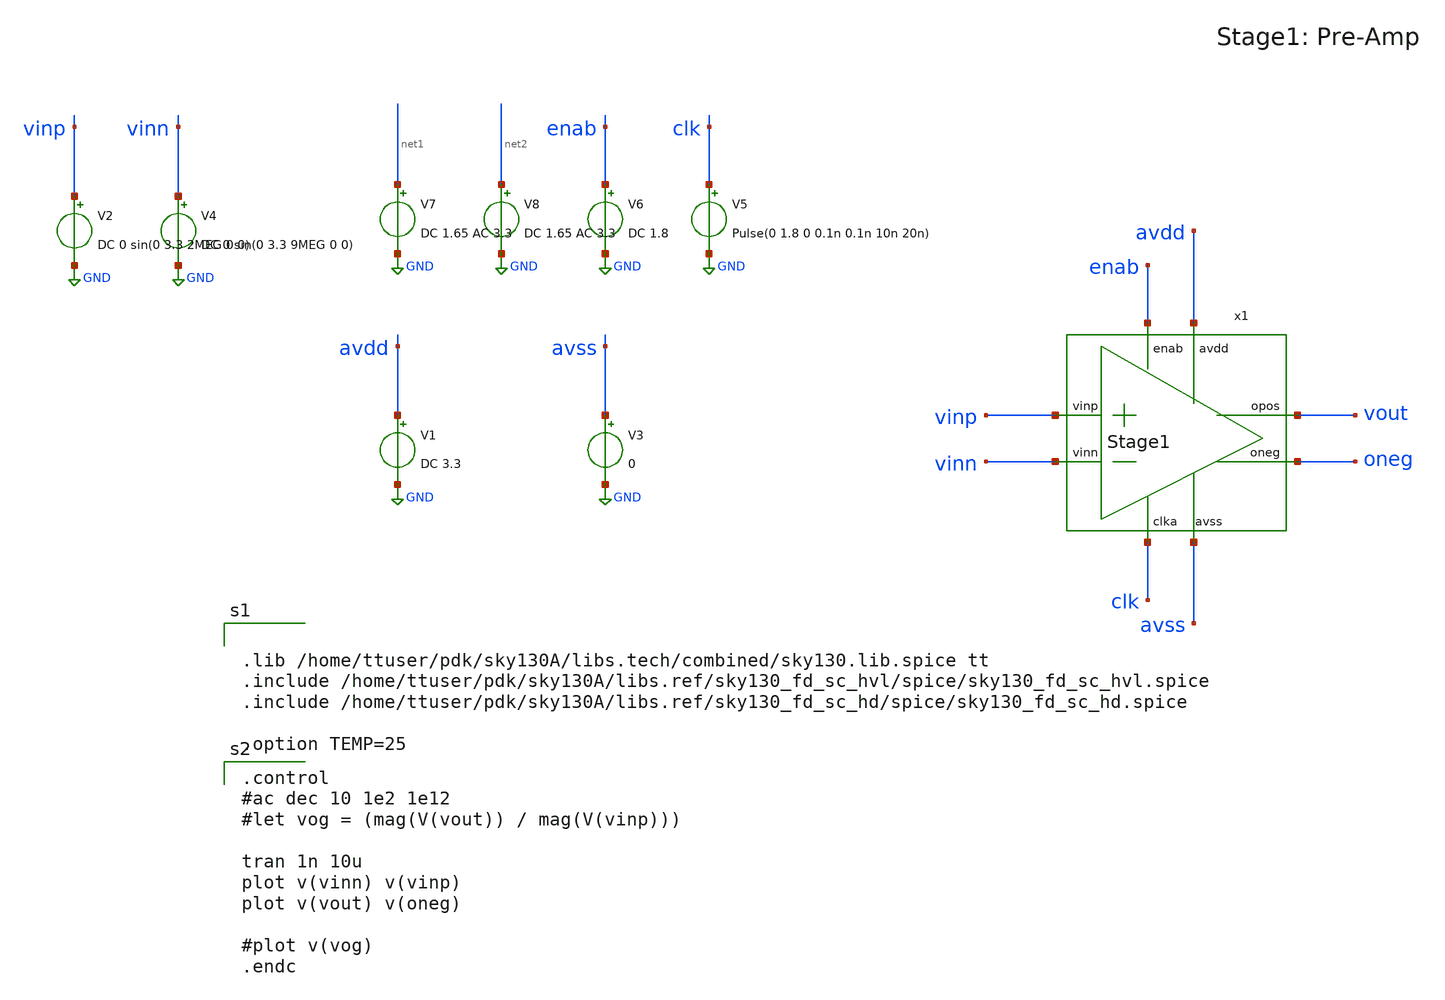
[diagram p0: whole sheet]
** sch_path: xschem/preamp.sch
**.subckt preamp
V1 avdd GND DC 3.3
V3 avss GND 0
V5 clk GND Pulse(0 1.8 0 0.1n 0.1n 10n 20n)
V6 enab GND DC 1.8
V7 net1 GND DC 1.65 AC 3.3
V8 net2 GND DC 1.65 AC 3.3
x1 avdd enab clk vinn vinp oneg vout avss Stage1
V2 vinp GND DC 0 sin(0 3.3 2MEG 0 0)
V4 vinn GND DC 0 sin(0 3.3 9MEG 0 0)
**** begin user architecture code


.lib /home/ttuser/pdk/sky130A/libs.tech/combined/sky130.lib.spice tt
.include /home/ttuser/pdk/sky130A/libs.ref/sky130_fd_sc_hvl/spice/sky130_fd_sc_hvl.spice
.include /home/ttuser/pdk/sky130A/libs.ref/sky130_fd_sc_hd/spice/sky130_fd_sc_hd.spice

.option TEMP=25


.control
#ac dec 10 1e2 1e12
#let vog = (mag(V(vout)) / mag(V(vinp)))

tran 1n 10u
plot v(vinn) v(vinp)
plot v(vout) v(oneg)

#plot v(vog)
.endc

**** end user architecture code
**.ends

* expanding   symbol:  Stage1.sym # of pins=8
** sym_path: xschem/Stage1.sym
** sch_path: xschem/Stage1.sch
.subckt Stage1 avdd enab clka vinn vinp oneg opos avss
*.ipin avdd
*.ipin vinp
*.ipin vinn
*.opin avss
*.opin opos
*.opin oneg
*.ipin clka
*.ipin enab
XM1 net4 net5 avdd avdd sky130_fd_pr__pfet_g5v0d10v5 L=1 W=50 nf=2 ad='int((nf+1)/2) * W/nf * 0.29' as='int((nf+2)/2) * W/nf * 0.29'
+ pd='2*int((nf+1)/2) * (W/nf + 0.29)' ps='2*int((nf+2)/2) * (W/nf + 0.29)' nrd='0.29 / W' nrs='0.29 / W'
+ sa=0 sb=0 sd=0 mult=2 m=2
x2 clka dvdd dvss dvss avdd avdd net2 sky130_fd_sc_hvl__lsbuflv2hv_1
XM6 net1 net2 net4 net4 sky130_fd_pr__pfet_g5v0d10v5 L=1 W=50 nf=2 ad='int((nf+1)/2) * W/nf * 0.29' as='int((nf+2)/2) * W/nf * 0.29'
+ pd='2*int((nf+1)/2) * (W/nf + 0.29)' ps='2*int((nf+2)/2) * (W/nf + 0.29)' nrd='0.29 / W' nrs='0.29 / W'
+ sa=0 sb=0 sd=0 mult=2 m=2
XM2 oneg vinp net1 net1 sky130_fd_pr__pfet_g5v0d10v5 L=1 W=20 nf=2 ad='int((nf+1)/2) * W/nf * 0.29' as='int((nf+2)/2) * W/nf * 0.29'
+ pd='2*int((nf+1)/2) * (W/nf + 0.29)' ps='2*int((nf+2)/2) * (W/nf + 0.29)' nrd='0.29 / W' nrs='0.29 / W'
+ sa=0 sb=0 sd=0 mult=2 m=2
XM3 opos vinn net1 net1 sky130_fd_pr__pfet_g5v0d10v5 L=1 W=20 nf=2 ad='int((nf+1)/2) * W/nf * 0.29' as='int((nf+2)/2) * W/nf * 0.29'
+ pd='2*int((nf+1)/2) * (W/nf + 0.29)' ps='2*int((nf+2)/2) * (W/nf + 0.29)' nrd='0.29 / W' nrs='0.29 / W'
+ sa=0 sb=0 sd=0 mult=2 m=2
XM4 net3 net3 avss avss sky130_fd_pr__nfet_03v3_nvt L=0.5 W=5 nf=1 ad='int((nf+1)/2) * W/nf * 0.29' as='int((nf+2)/2) * W/nf * 0.29'
+ pd='2*int((nf+1)/2) * (W/nf + 0.29)' ps='2*int((nf+2)/2) * (W/nf + 0.29)' nrd='0.29 / W' nrs='0.29 / W'
+ sa=0 sb=0 sd=0 mult=2 m=2
XM8 opos net2 net3 net3 sky130_fd_pr__nfet_g5v0d10v5 L=0.5 W=5 nf=1 ad='int((nf+1)/2) * W/nf * 0.29'
+ as='int((nf+2)/2) * W/nf * 0.29' pd='2*int((nf+1)/2) * (W/nf + 0.29)' ps='2*int((nf+2)/2) * (W/nf + 0.29)'
+ nrd='0.29 / W' nrs='0.29 / W' sa=0 sb=0 sd=0 mult=1 m=1
XM5 oneg net2 net3 net3 sky130_fd_pr__nfet_g5v0d10v5 L=0.5 W=5 nf=1 ad='int((nf+1)/2) * W/nf * 0.29'
+ as='int((nf+2)/2) * W/nf * 0.29' pd='2*int((nf+1)/2) * (W/nf + 0.29)' ps='2*int((nf+2)/2) * (W/nf + 0.29)'
+ nrd='0.29 / W' nrs='0.29 / W' sa=0 sb=0 sd=0 mult=1 m=1
x1 enab dvdd dvss dvss avdd avdd net5 sky130_fd_sc_hvl__lsbuflv2hv_1
.ends

.GLOBAL GND
.end
